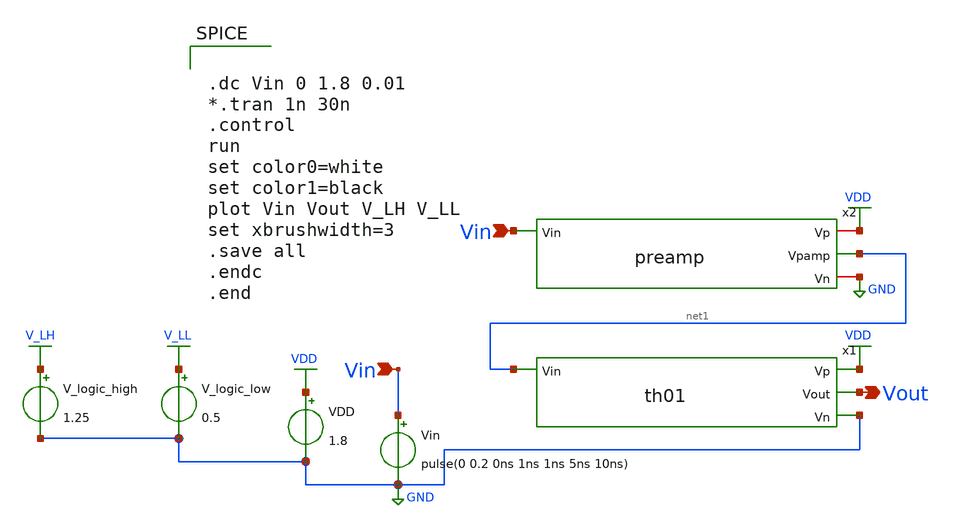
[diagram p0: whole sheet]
** sch_path: xschem/Vth_sch/Pre_layout/th01_1.sch
**.subckt th01_1 Vin Vout Vin
*.ipin Vin
*.opin Vout
*.ipin Vin
VDD VDD GND 1.8
Vin Vin GND pulse(0 0.2 0ns 1ns 1ns 5ns 10ns)
V_logic_high V_LH GND 1.25
V_logic_low V_LL GND 0.5
x2 VDD Vin net1 GND preamp
x1 VDD net1 Vout GND th01
**** begin user architecture code


.lib /usr/local/share/pdk/sky130A/libs.tech/ngspice/sky130.lib.spice tt

.save all





.dc Vin 0 1.8 0.01
*.tran 1n 30n
.control
run
set color0=white
set color1=black
plot Vin Vout V_LH V_LL
set xbrushwidth=3
.save all
.endc
.end


**** end user architecture code
**.ends

* expanding   symbol:  /home/exotic/Desktop/ASIC_ADC/xschem/Vth_sch/Symbol/preamp.sym # of pins=4
** sym_path: xschem/Vth_sch/Symbol/preamp.sym
** sch_path: xschem/Vth_sch/Symbol/preamp.sch
.subckt preamp Vp Vin Vpamp Vn
*.ipin Vin
*.opin Vpamp
*.iopin Vp
*.iopin Vn
XM1 Vp Vin Vpamp Vpamp sky130_fd_pr__nfet_01v8 L=0.15 W=0.42 nf=1 ad='int((nf+1)/2) * W/nf * 0.29' as='int((nf+2)/2) * W/nf * 0.29'
+ pd='2*int((nf+1)/2) * (W/nf + 0.29)' ps='2*int((nf+2)/2) * (W/nf + 0.29)' nrd='0.29 / W' nrs='0.29 / W'
+ sa=0 sb=0 sd=0 mult=1 m=1
XM0 Vn Vin Vpamp Vpamp sky130_fd_pr__pfet_01v8 L=3.25 W=0.42 nf=1 ad='int((nf+1)/2) * W/nf * 0.29' as='int((nf+2)/2) * W/nf * 0.29'
+ pd='2*int((nf+1)/2) * (W/nf + 0.29)' ps='2*int((nf+2)/2) * (W/nf + 0.29)' nrd='0.29 / W' nrs='0.29 / W'
+ sa=0 sb=0 sd=0 mult=1 m=1
.ends


* expanding   symbol:  /home/exotic/Desktop/ASIC_ADC/xschem/Vth_sch/Symbol/th01.sym # of pins=4
** sym_path: xschem/Vth_sch/Symbol/th01.sym
** sch_path: xschem/Vth_sch/Symbol/th01.sch
.subckt th01 Vp Vin Vout Vn
*.ipin Vin
*.opin Vout
*.iopin Vp
*.iopin Vn
XM5 Vout net1 Vp Vp sky130_fd_pr__pfet_01v8 L=0.15 W=3.1 nf=1 ad='int((nf+1)/2) * W/nf * 0.29' as='int((nf+2)/2) * W/nf * 0.29'
+ pd='2*int((nf+1)/2) * (W/nf + 0.29)' ps='2*int((nf+2)/2) * (W/nf + 0.29)' nrd='0.29 / W' nrs='0.29 / W'
+ sa=0 sb=0 sd=0 mult=1 m=1
XM4 Vout net1 Vn Vn sky130_fd_pr__nfet_01v8 L=2.97 W=0.48 nf=1 ad='int((nf+1)/2) * W/nf * 0.29' as='int((nf+2)/2) * W/nf * 0.29'
+ pd='2*int((nf+1)/2) * (W/nf + 0.29)' ps='2*int((nf+2)/2) * (W/nf + 0.29)' nrd='0.29 / W' nrs='0.29 / W'
+ sa=0 sb=0 sd=0 mult=1 m=1
XM2 net1 Vin Vp Vp sky130_fd_pr__pfet_01v8 L=2.96 W=0.42 nf=1 ad='int((nf+1)/2) * W/nf * 0.29' as='int((nf+2)/2) * W/nf * 0.29'
+ pd='2*int((nf+1)/2) * (W/nf + 0.29)' ps='2*int((nf+2)/2) * (W/nf + 0.29)' nrd='0.29 / W' nrs='0.29 / W'
+ sa=0 sb=0 sd=0 mult=1 m=1
XM3 net1 Vin Vn Vn sky130_fd_pr__nfet_01v8 L=0.15 W=3.1 nf=1 ad='int((nf+1)/2) * W/nf * 0.29' as='int((nf+2)/2) * W/nf * 0.29'
+ pd='2*int((nf+1)/2) * (W/nf + 0.29)' ps='2*int((nf+2)/2) * (W/nf + 0.29)' nrd='0.29 / W' nrs='0.29 / W'
+ sa=0 sb=0 sd=0 mult=1 m=1
.ends

.GLOBAL VDD
.GLOBAL GND
.GLOBAL V_LH
.GLOBAL V_LL
.end
